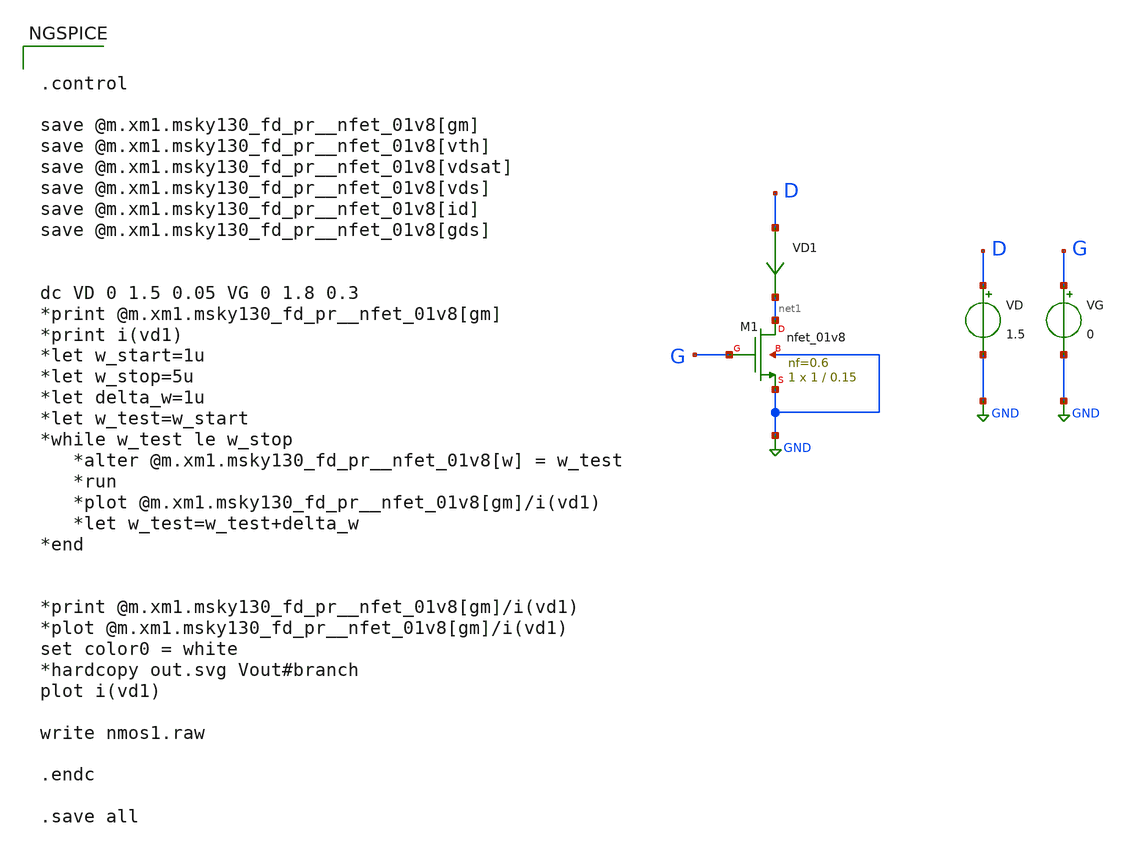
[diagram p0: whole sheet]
** sch_path: nmos1.sch
**.subckt nmos1
VD1 D net1 0
.save i(vd1)
VD D GND 1.5
VG G GND 0
XM1 net1 G GND GND sky130_fd_pr__nfet_01v8 L=0.15 W=1 nf=0.6 ad='int((nf+1)/2) * W/nf * 0.29' as='int((nf+2)/2) * W/nf * 0.29'
+ pd='2*int((nf+1)/2) * (W/nf + 0.29)' ps='2*int((nf+2)/2) * (W/nf + 0.29)' nrd='0.29 / W' nrs='0.29 / W'
+ sa=0 sb=0 sd=0 mult=1 m=1
**** begin user architecture code


.control

save @m.xm1.msky130_fd_pr__nfet_01v8[gm]
save @m.xm1.msky130_fd_pr__nfet_01v8[vth]
save @m.xm1.msky130_fd_pr__nfet_01v8[vdsat]
save @m.xm1.msky130_fd_pr__nfet_01v8[vds]
save @m.xm1.msky130_fd_pr__nfet_01v8[id]
save @m.xm1.msky130_fd_pr__nfet_01v8[gds]


dc VD 0 1.5 0.05 VG 0 1.8 0.3
*print @m.xm1.msky130_fd_pr__nfet_01v8[gm]
*print i(vd1)
*let w_start=1u
*let w_stop=5u
*let delta_w=1u
*let w_test=w_start
*while w_test le w_stop
   *alter @m.xm1.msky130_fd_pr__nfet_01v8[w] = w_test
   *run
   *plot @m.xm1.msky130_fd_pr__nfet_01v8[gm]/i(vd1)
   *let w_test=w_test+delta_w
*end


*print @m.xm1.msky130_fd_pr__nfet_01v8[gm]/i(vd1)
*plot @m.xm1.msky130_fd_pr__nfet_01v8[gm]/i(vd1)
set color0 = white
*hardcopy out.svg Vout#branch
plot i(vd1)

write nmos1.raw

.endc

.save all



** opencircuitdesign pdks install
.lib $::SKYWATER_MODELS/sky130.lib.spice tt


**** end user architecture code
**.ends
.GLOBAL GND
.end
